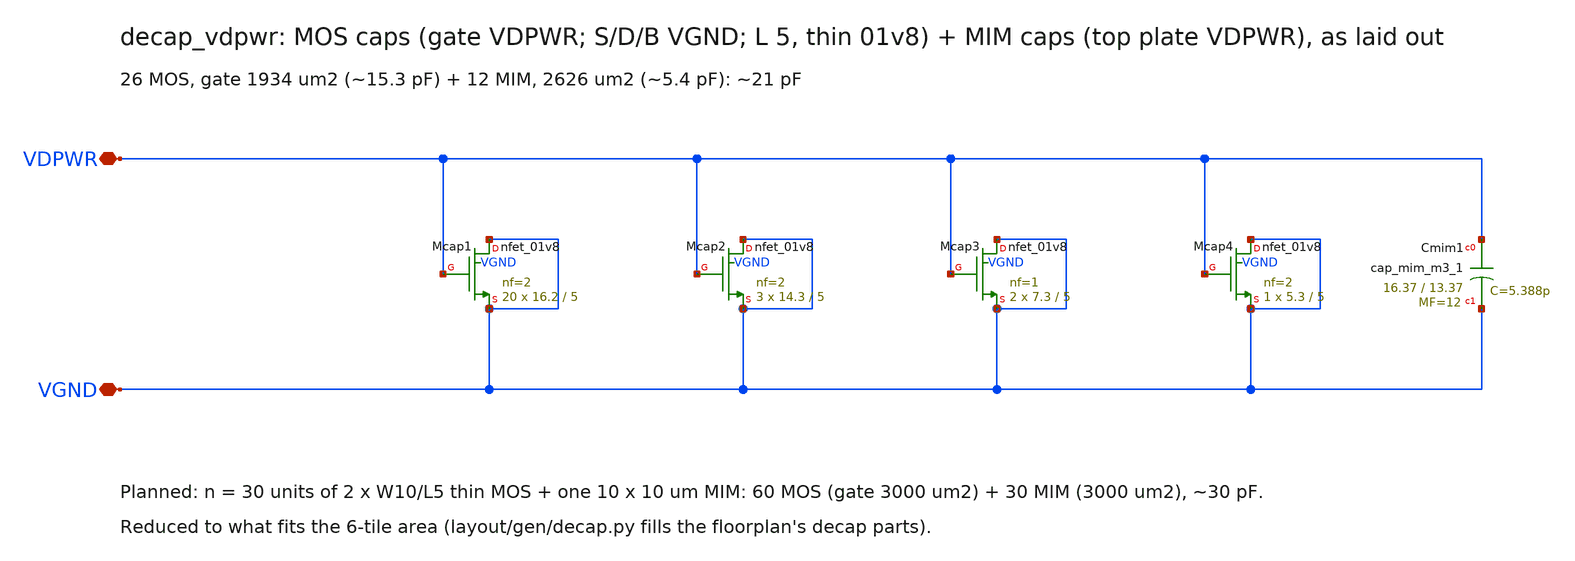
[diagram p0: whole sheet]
** sch_path: xschem/decap_vdpwr.sch
**.subckt decap_vdpwr VDPWR VGND
*.iopin VDPWR
*.iopin VGND
XMcap1 VGND VDPWR VGND VGND sky130_fd_pr__nfet_01v8 L=5 W=16.2 nf=2 ad='int((nf+1)/2) * W/nf * 0.29'
+ as='int((nf+2)/2) * W/nf * 0.29' pd='2*int((nf+1)/2) * (W/nf + 0.29)' ps='2*int((nf+2)/2) * (W/nf + 0.29)'
+ nrd='0.29 / W' nrs='0.29 / W' sa=0 sb=0 sd=0 mult=20 m=20
XMcap2 VGND VDPWR VGND VGND sky130_fd_pr__nfet_01v8 L=5 W=14.3 nf=2 ad='int((nf+1)/2) * W/nf * 0.29'
+ as='int((nf+2)/2) * W/nf * 0.29' pd='2*int((nf+1)/2) * (W/nf + 0.29)' ps='2*int((nf+2)/2) * (W/nf + 0.29)'
+ nrd='0.29 / W' nrs='0.29 / W' sa=0 sb=0 sd=0 mult=3 m=3
XMcap3 VGND VDPWR VGND VGND sky130_fd_pr__nfet_01v8 L=5 W=7.3 nf=1 ad='int((nf+1)/2) * W/nf * 0.29' as='int((nf+2)/2) * W/nf * 0.29'
+ pd='2*int((nf+1)/2) * (W/nf + 0.29)' ps='2*int((nf+2)/2) * (W/nf + 0.29)' nrd='0.29 / W' nrs='0.29 / W'
+ sa=0 sb=0 sd=0 mult=2 m=2
XMcap4 VGND VDPWR VGND VGND sky130_fd_pr__nfet_01v8 L=5 W=5.3 nf=2 ad='int((nf+1)/2) * W/nf * 0.29' as='int((nf+2)/2) * W/nf * 0.29'
+ pd='2*int((nf+1)/2) * (W/nf + 0.29)' ps='2*int((nf+2)/2) * (W/nf + 0.29)' nrd='0.29 / W' nrs='0.29 / W'
+ sa=0 sb=0 sd=0 mult=1 m=1
XCmim1 VDPWR VGND sky130_fd_pr__cap_mim_m3_1 W=16.37 L=13.37 MF=12 m=12
**.ends
.end
